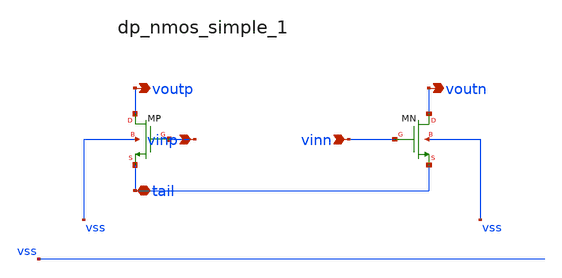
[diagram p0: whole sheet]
** sch_path: analog-db/raw/dp_001_resistive_load/hier/blocks/dp_nmos_simple_1.sch
**.subckt dp_nmos_simple_1 vinp vinn tail voutp voutn
*.ipin vinp
*.ipin vinn
*.iopin tail
*.opin voutp
*.opin voutn
XMN voutn vinn tail vss sg13_lv_nmos w=x_dut_xmn_w l=x_dut_xmn_l ng=1 m=x_dut_xmn_m
XMP voutp vinp tail vss sg13_lv_nmos w=x_dut_xmp_w l=x_dut_xmp_l ng=1 m=x_dut_xmp_m
**.ends
.end
